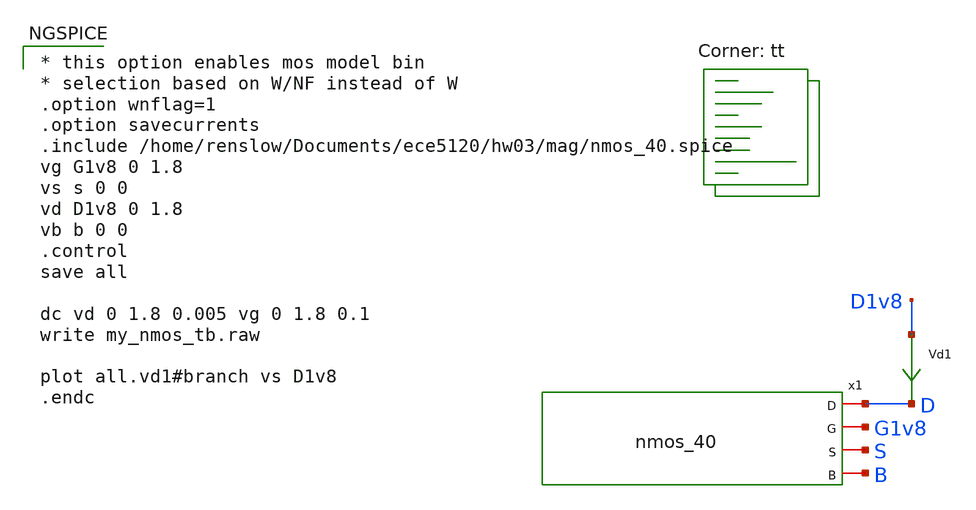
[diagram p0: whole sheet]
** sch_path: hw03/mag/nmos_tb.sch
**.subckt nmos_tb
Vd1 D1v8 D 0
.save i(vd1)
x1 D G1v8 S B nmos_40
**** begin user architecture code

* this option enables mos model bin
* selection based on W/NF instead of W
.option wnflag=1
.option savecurrents
.include /home/renslow/Documents/ece5120/hw03/mag/nmos_40.spice
vg G1v8 0 1.8
vs s 0 0
vd D1v8 0 1.8
vb b 0 0
.control
save all

dc vd 0 1.8 0.005 vg 0 1.8 0.1
write my_nmos_tb.raw

plot all.vd1#branch vs D1v8
.endc


.lib $::SKYWATER_MODELS/sky130.lib.spice tt
**** end user architecture code
**.ends
.end
